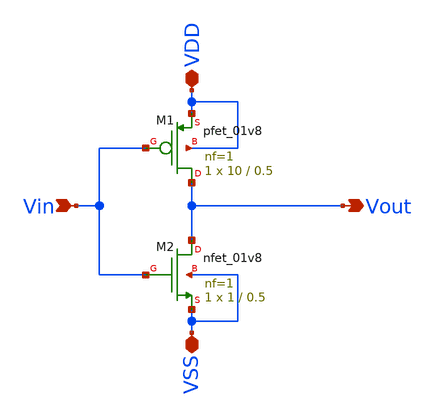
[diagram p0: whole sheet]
** sch_path: EEE351_inv.sch
**.subckt EEE351_inv Vin VSS VDD Vout
*.ipin Vin
*.iopin VSS
*.iopin VDD
*.opin Vout
XM1 Vout Vin VDD VDD sky130_fd_pr__pfet_01v8 L=0.5 W=10 nf=1 ad='int((nf+1)/2) * W/nf * 0.29' as='int((nf+2)/2) * W/nf * 0.29'
+ pd='2*int((nf+1)/2) * (W/nf + 0.29)' ps='2*int((nf+2)/2) * (W/nf + 0.29)' nrd='0.29 / W' nrs='0.29 / W'
+ sa=0 sb=0 sd=0 mult=1 m=1
XM2 Vout Vin VSS VSS sky130_fd_pr__nfet_01v8 L=0.5 W=1 nf=1 ad='int((nf+1)/2) * W/nf * 0.29' as='int((nf+2)/2) * W/nf * 0.29'
+ pd='2*int((nf+1)/2) * (W/nf + 0.29)' ps='2*int((nf+2)/2) * (W/nf + 0.29)' nrd='0.29 / W' nrs='0.29 / W'
+ sa=0 sb=0 sd=0 mult=1 m=1
**.ends
.end
